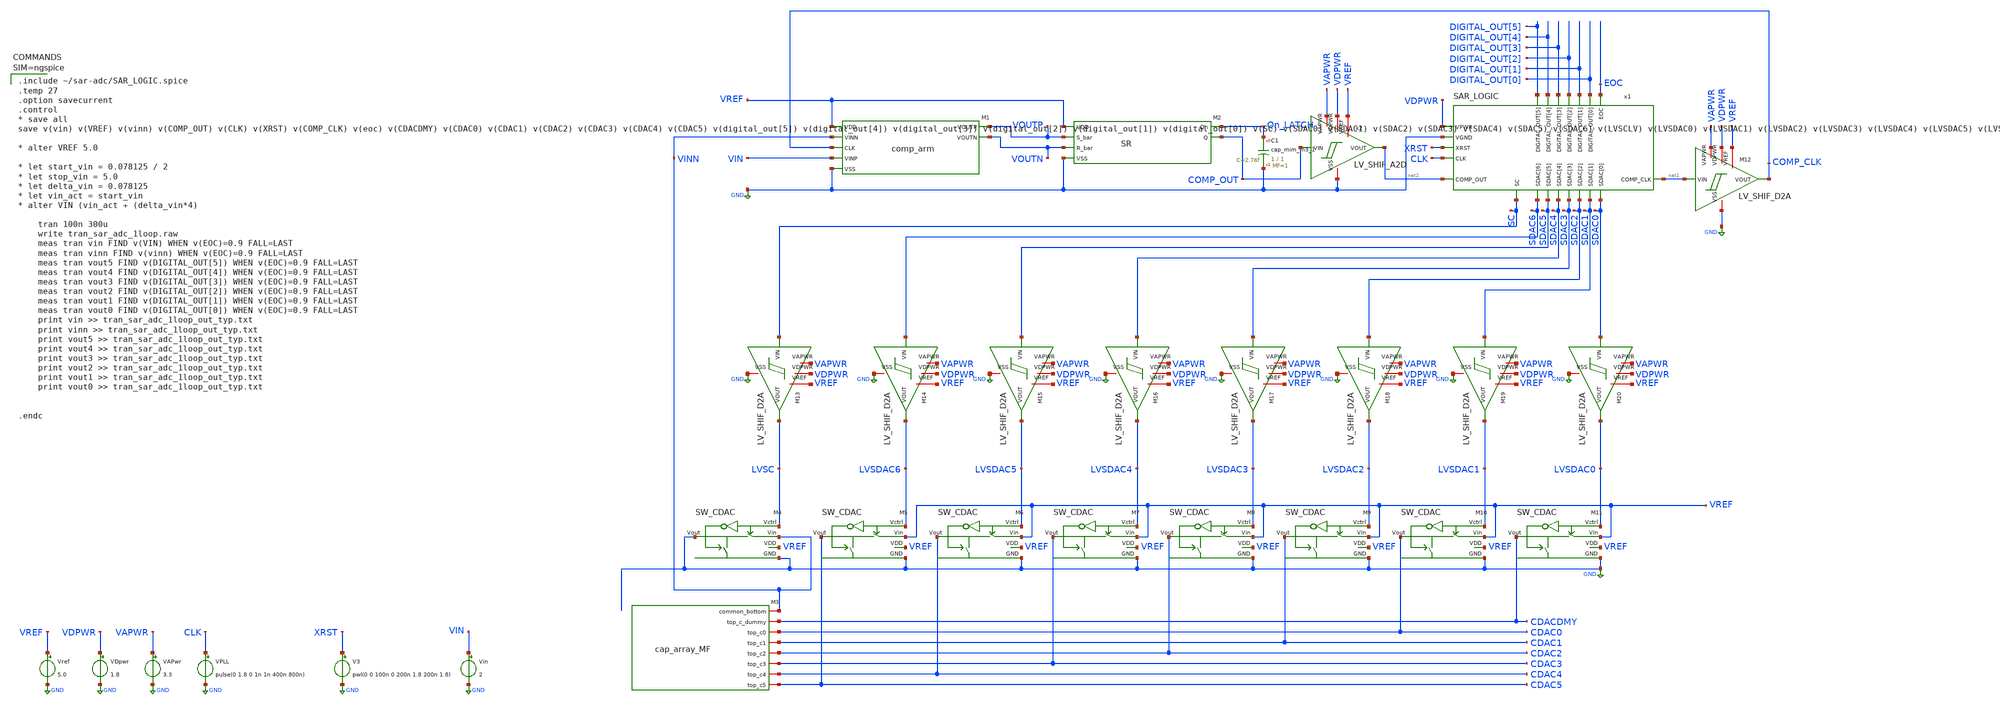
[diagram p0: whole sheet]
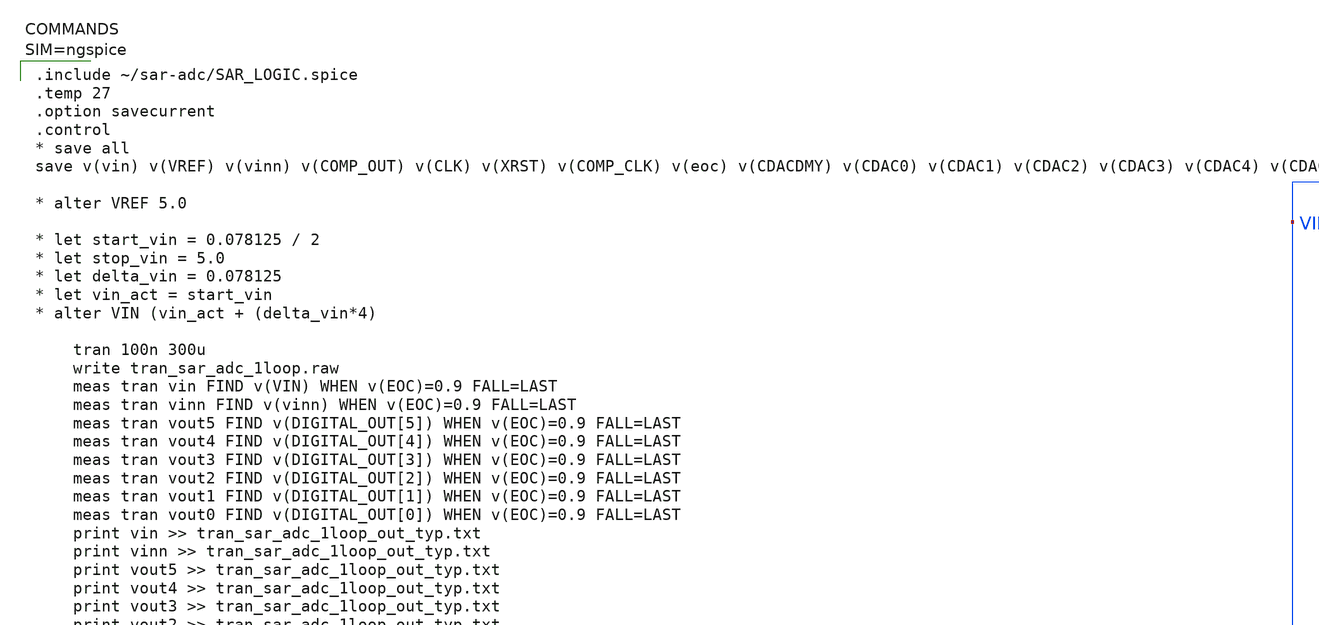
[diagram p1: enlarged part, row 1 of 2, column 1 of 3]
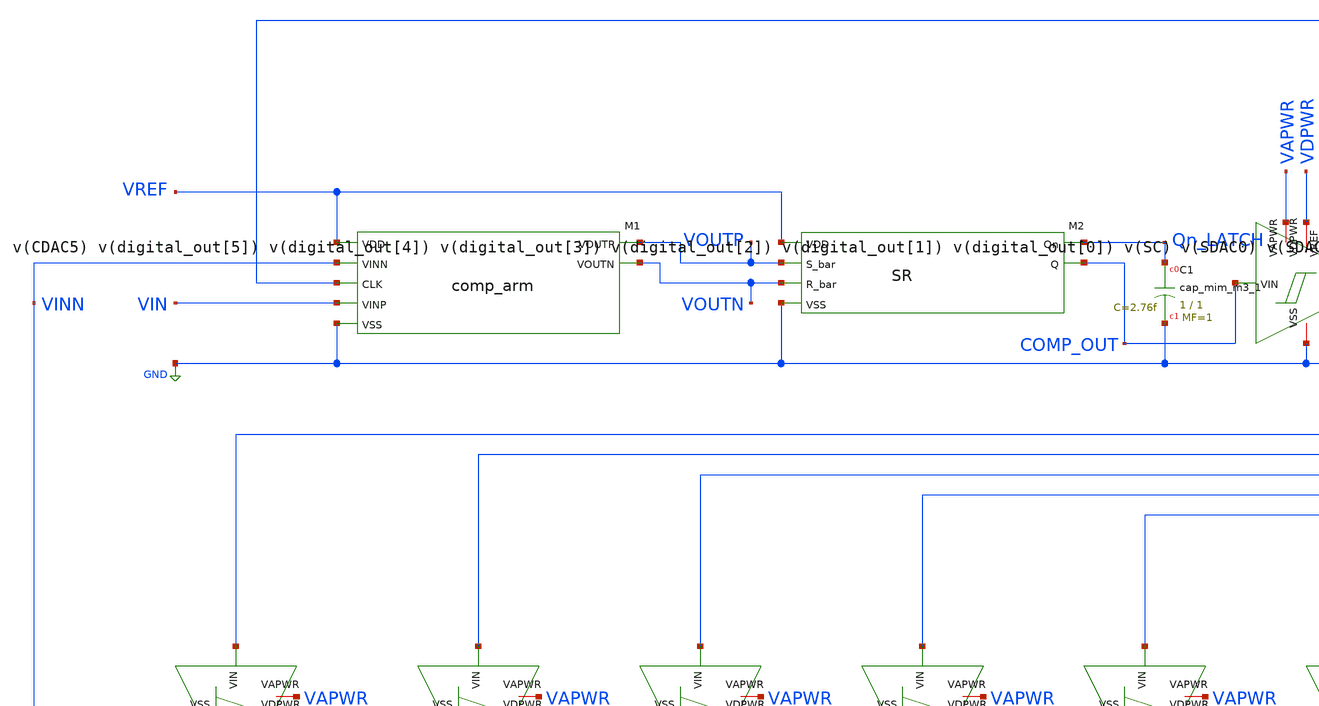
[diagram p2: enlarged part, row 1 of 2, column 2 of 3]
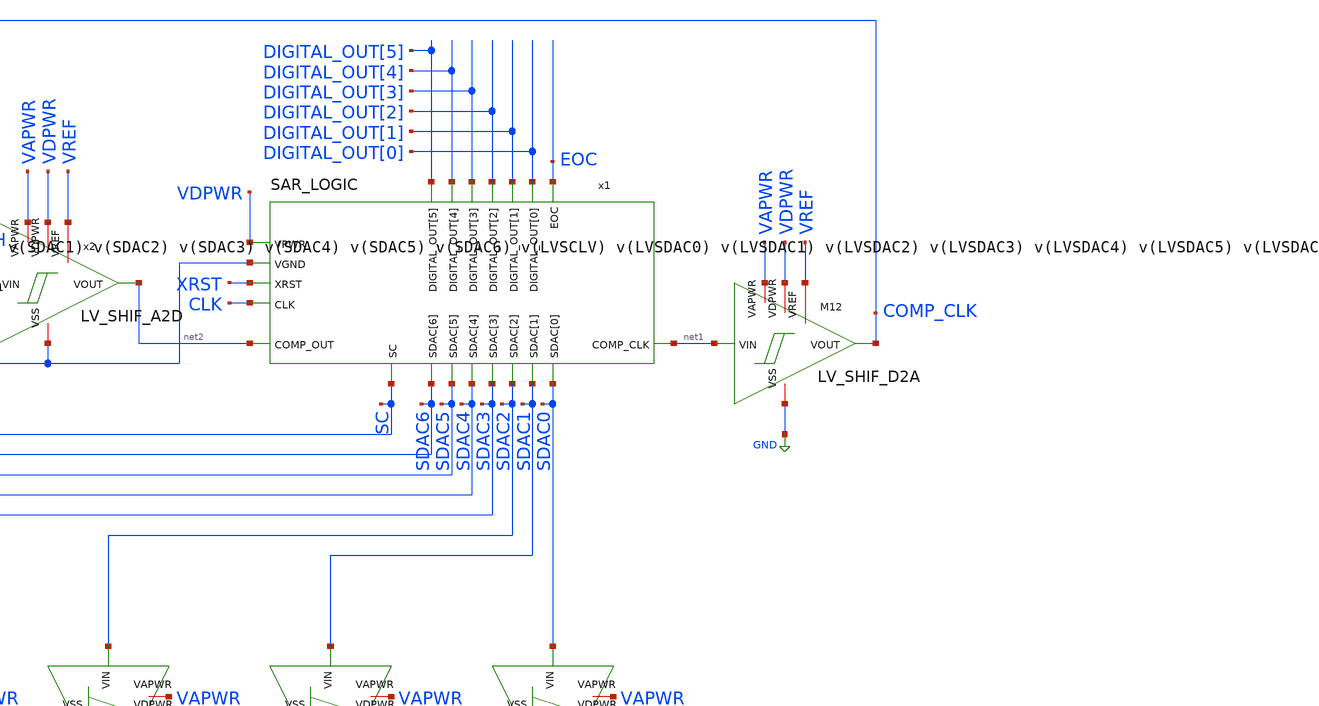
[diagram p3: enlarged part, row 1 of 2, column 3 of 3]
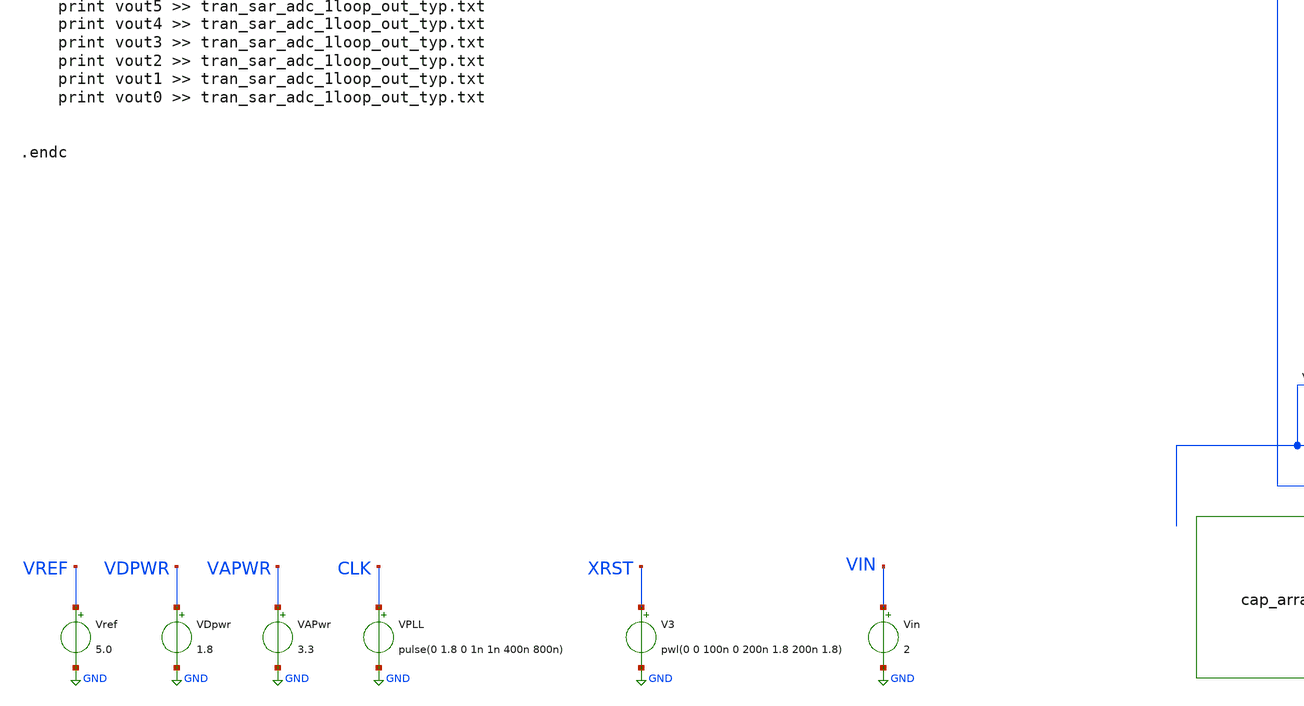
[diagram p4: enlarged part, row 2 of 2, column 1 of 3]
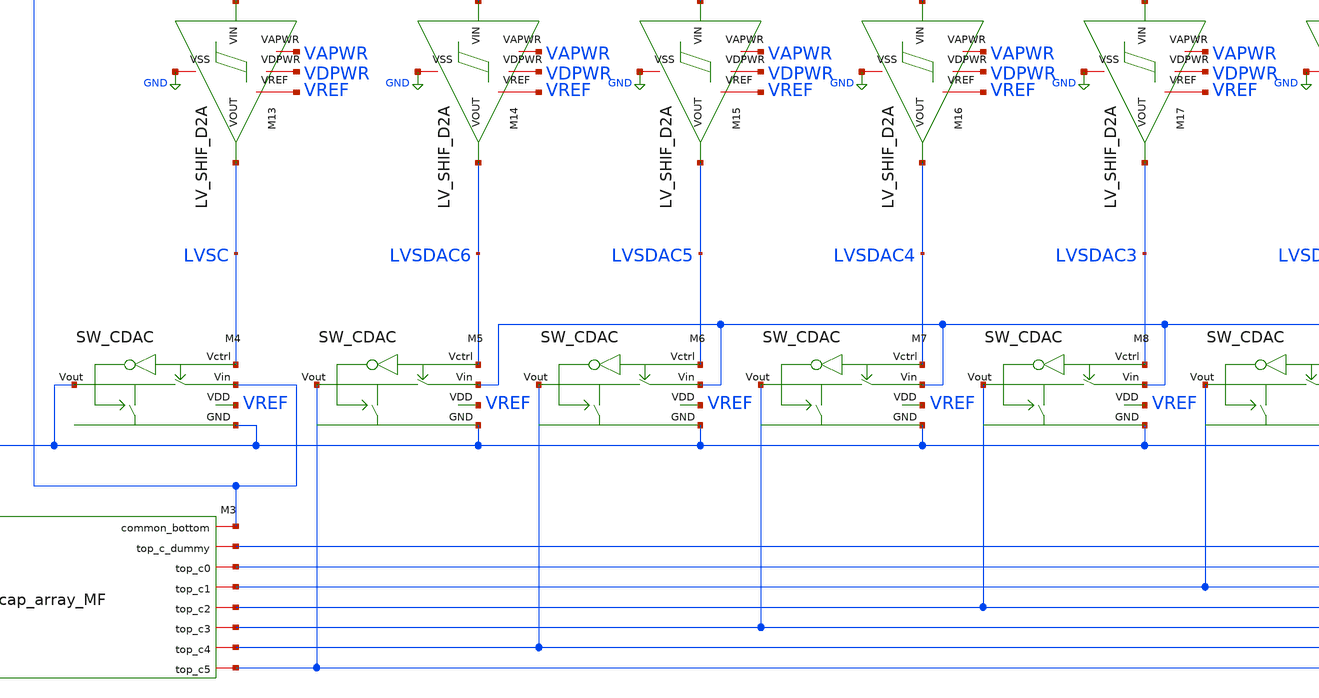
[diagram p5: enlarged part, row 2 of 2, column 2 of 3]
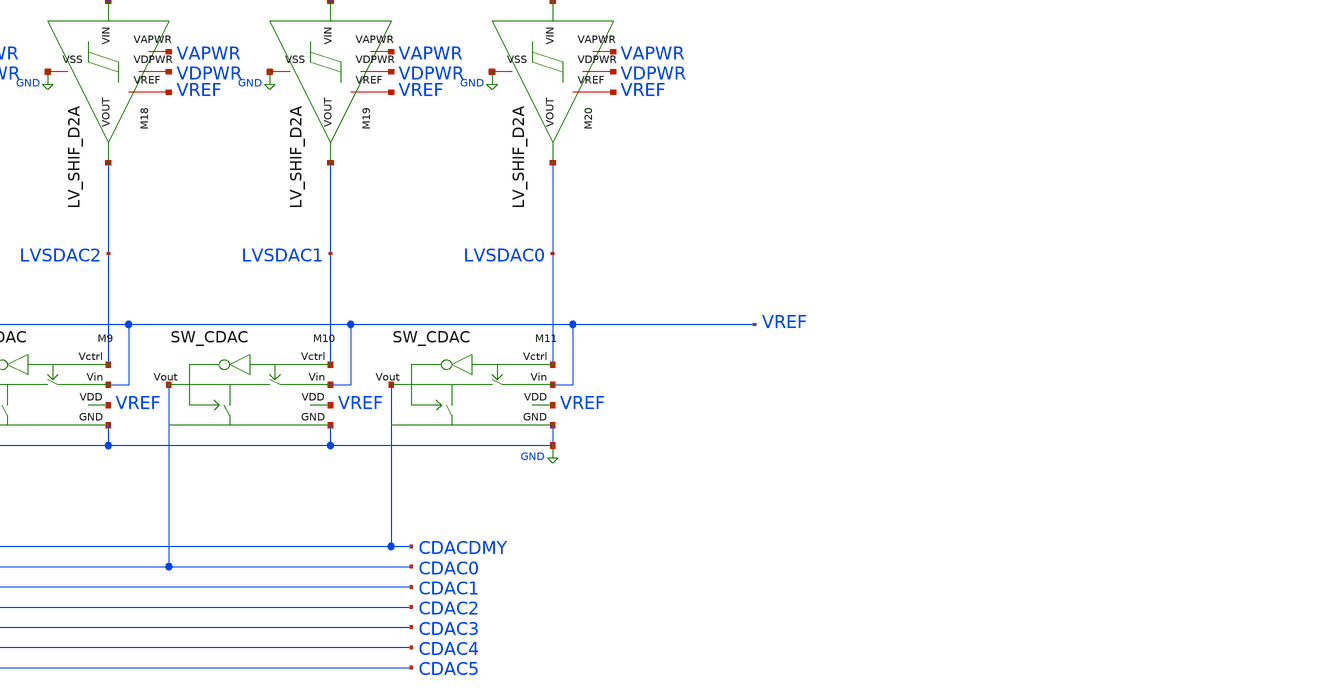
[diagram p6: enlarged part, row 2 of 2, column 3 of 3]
** sch_path: SKY130/SAR-ADC/SAR-ADC_5.0V/tran_sar_adc_1loop_arm.sch
**.subckt tran_sar_adc_1loop_arm
VAPwr VAPWR GND 3.3
Vin VIN GND 2
Vref VREF GND 5.0
VDpwr VDPWR GND 1.8
XM2 VREF Qn_LATCH COMP_OUT VOUTN VOUTP GND SR
x1 CLK net1 net2 DIGITAL_OUT[0] DIGITAL_OUT[1] DIGITAL_OUT[2] DIGITAL_OUT[3] DIGITAL_OUT[4]
+ DIGITAL_OUT[5] EOC SC SDAC0 SDAC1 SDAC2 SDAC3 SDAC4 SDAC5 SDAC6 GND VDPWR XRST SAR_LOGIC
XM4 VREF LVSC GND GND VINN SW_CDAC
XM5 VREF LVSDAC6 GND CDAC5 VREF SW_CDAC
XM6 VREF LVSDAC5 GND CDAC4 VREF SW_CDAC
XM7 VREF LVSDAC4 GND CDAC3 VREF SW_CDAC
XM8 VREF LVSDAC3 GND CDAC2 VREF SW_CDAC
XM9 VREF LVSDAC2 GND CDAC1 VREF SW_CDAC
XM10 VREF LVSDAC1 GND CDAC0 VREF SW_CDAC
XM11 VREF LVSDAC0 GND CDACDMY VREF SW_CDAC
XC1 Qn_LATCH GND sky130_fd_pr__cap_mim_m3_1 W=1 L=1 MF=1 m=1
XM12 VAPWR VDPWR VREF COMP_CLK net1 GND LV_SHIF_D2A
XM13 VAPWR VDPWR VREF LVSC SC GND LV_SHIF_D2A
XM14 VAPWR VDPWR VREF LVSDAC6 SDAC6 GND LV_SHIF_D2A
XM15 VAPWR VDPWR VREF LVSDAC5 SDAC5 GND LV_SHIF_D2A
XM16 VAPWR VDPWR VREF LVSDAC4 SDAC4 GND LV_SHIF_D2A
XM17 VAPWR VDPWR VREF LVSDAC3 SDAC3 GND LV_SHIF_D2A
XM18 VAPWR VDPWR VREF LVSDAC2 SDAC2 GND LV_SHIF_D2A
XM19 VAPWR VDPWR VREF LVSDAC1 SDAC1 GND LV_SHIF_D2A
XM20 VAPWR VDPWR VREF LVSDAC0 SDAC0 GND LV_SHIF_D2A
Xx2 VAPWR VDPWR VREF net2 COMP_OUT GND LV_SHIF_A2D
XM3 VINN CDAC5 CDAC0 CDAC2 CDAC4 CDAC3 CDACDMY CDAC1 cap_array_MF
VPLL CLK GND pulse(0 1.8 0 1n 1n 400n 800n)
V3 XRST GND pwl(0 0 100n 0 200n 1.8 200n 1.8)
XM1 VOUTP VREF VIN VINN COMP_CLK GND VOUTN comp_arm
**** begin user architecture code


.include ~/sar-adc/SAR_LOGIC.spice
.temp 27
.option savecurrent
.control
* save all
save v(vin) v(VREF) v(vinn) v(COMP_OUT) v(CLK) v(XRST) v(COMP_CLK) v(eoc) v(CDACDMY) v(CDAC0)
+ v(CDAC1) v(CDAC2) v(CDAC3) v(CDAC4) v(CDAC5) v(digital_out[5]) v(digital_out[4]) v(digital_out[3])
+ v(digital_out[2]) v(digital_out[1]) v(digital_out[0]) v(SC) v(SDAC0) v(SDAC1) v(SDAC2) v(SDAC3) v(SDAC4) v(SDAC5)
+ v(SDAC6) v(LVSCLV) v(LVSDAC0) v(LVSDAC1) v(LVSDAC2) v(LVSDAC3) v(LVSDAC4) v(LVSDAC5) v(LVSDAC6)

* alter VREF 5.0

* let start_vin = 0.078125 / 2
* let stop_vin = 5.0
* let delta_vin = 0.078125
* let vin_act = start_vin
* alter VIN (vin_act + (delta_vin*4)

	tran 100n 300u
	write tran_sar_adc_1loop.raw
	meas tran vin FIND v(VIN) WHEN v(EOC)=0.9 FALL=LAST
	meas tran vinn FIND v(vinn) WHEN v(EOC)=0.9 FALL=LAST
	meas tran vout5 FIND v(DIGITAL_OUT[5]) WHEN v(EOC)=0.9 FALL=LAST
	meas tran vout4 FIND v(DIGITAL_OUT[4]) WHEN v(EOC)=0.9 FALL=LAST
	meas tran vout3 FIND v(DIGITAL_OUT[3]) WHEN v(EOC)=0.9 FALL=LAST
	meas tran vout2 FIND v(DIGITAL_OUT[2]) WHEN v(EOC)=0.9 FALL=LAST
	meas tran vout1 FIND v(DIGITAL_OUT[1]) WHEN v(EOC)=0.9 FALL=LAST
	meas tran vout0 FIND v(DIGITAL_OUT[0]) WHEN v(EOC)=0.9 FALL=LAST
	print vin >> tran_sar_adc_1loop_out_typ.txt
	print vinn >> tran_sar_adc_1loop_out_typ.txt
	print vout5 >> tran_sar_adc_1loop_out_typ.txt
	print vout4 >> tran_sar_adc_1loop_out_typ.txt
	print vout3 >> tran_sar_adc_1loop_out_typ.txt
	print vout2 >> tran_sar_adc_1loop_out_typ.txt
	print vout1 >> tran_sar_adc_1loop_out_typ.txt
	print vout0 >> tran_sar_adc_1loop_out_typ.txt


.endc




** opencircuitdesign pdks install
.lib $::SKYWATER_MODELS/sky130.lib.spice tt

**** end user architecture code
**.ends
.GLOBAL GND
.end
